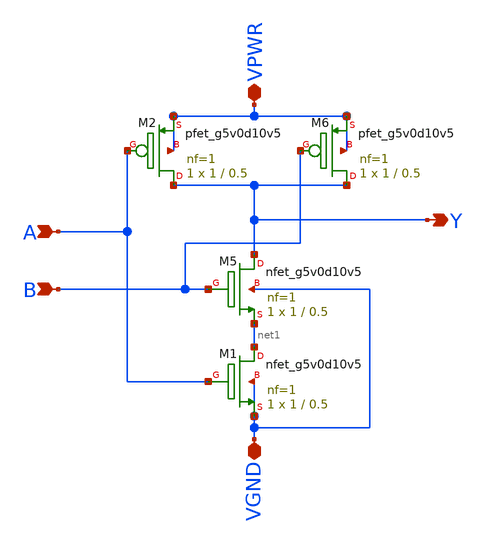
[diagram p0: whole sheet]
** sch_path: my_nand_2.sch
**.subckt my_nand_2 VPWR VGND A B Y
*.iopin VPWR
*.iopin VGND
*.ipin A
*.ipin B
*.opin Y
XM5 Y B net1 VGND sky130_fd_pr__nfet_g5v0d10v5 L=0.5 W=1 nf=1 ad='int((nf+1)/2) * W/nf * 0.29' as='int((nf+2)/2) * W/nf * 0.29'
+ pd='2*int((nf+1)/2) * (W/nf + 0.29)' ps='2*int((nf+2)/2) * (W/nf + 0.29)' nrd='0.29 / W' nrs='0.29 / W'
+ sa=0 sb=0 sd=0 mult=1 m=1
XM6 Y B VPWR VPWR sky130_fd_pr__pfet_g5v0d10v5 L=0.5 W=1 nf=1 ad='int((nf+1)/2) * W/nf * 0.29' as='int((nf+2)/2) * W/nf * 0.29'
+ pd='2*int((nf+1)/2) * (W/nf + 0.29)' ps='2*int((nf+2)/2) * (W/nf + 0.29)' nrd='0.29 / W' nrs='0.29 / W'
+ sa=0 sb=0 sd=0 mult=1 m=1
XM2 Y A VPWR VPWR sky130_fd_pr__pfet_g5v0d10v5 L=0.5 W=1 nf=1 ad='int((nf+1)/2) * W/nf * 0.29' as='int((nf+2)/2) * W/nf * 0.29'
+ pd='2*int((nf+1)/2) * (W/nf + 0.29)' ps='2*int((nf+2)/2) * (W/nf + 0.29)' nrd='0.29 / W' nrs='0.29 / W'
+ sa=0 sb=0 sd=0 mult=1 m=1
XM1 net1 A VGND VGND sky130_fd_pr__nfet_g5v0d10v5 L=0.5 W=1 nf=1 ad='int((nf+1)/2) * W/nf * 0.29' as='int((nf+2)/2) * W/nf * 0.29'
+ pd='2*int((nf+1)/2) * (W/nf + 0.29)' ps='2*int((nf+2)/2) * (W/nf + 0.29)' nrd='0.29 / W' nrs='0.29 / W'
+ sa=0 sb=0 sd=0 mult=1 m=1
**.ends
.end
